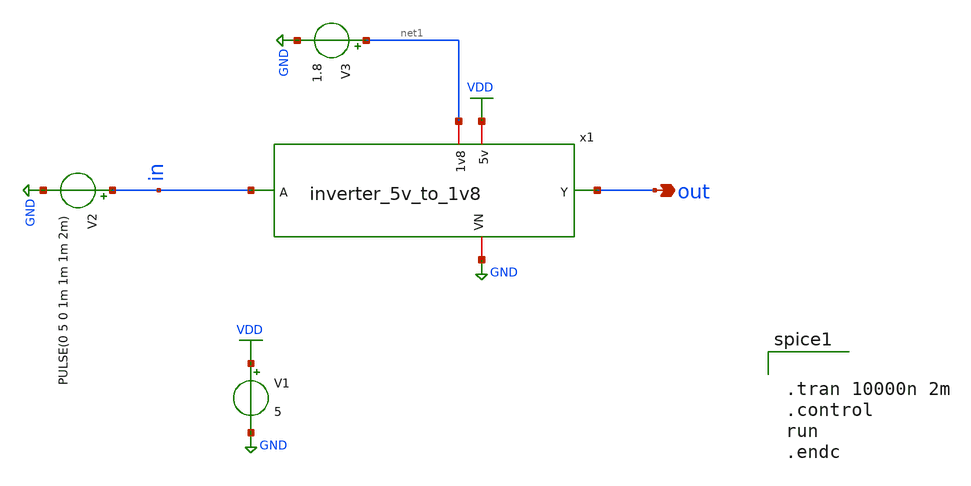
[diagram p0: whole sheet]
** sch_path: ADC/16bit_C2C/MagicAndSpice/inverter_5v_to_1v8_TB.sch
**.subckt inverter_5v_to_1v8_TB out
*.opin out
V1 VDD GND 5
V2 in GND PULSE(0 5 0 1m 1m 1m 2m)
x1 net1 VDD out in GND inverter_5v_to_1v8
V3 net1 GND 1.8
**** begin user architecture code
 .lib $::SKYWATER_MODELS/sky130.lib.spice tt


.tran 10000n 2m
.control
run
.endc

**** end user architecture code
**.ends

* expanding   symbol:  /home/ee431/workspace/6SAR_CDAC/inverter_5v_to_1v8.sym # of pins=5
** sym_path: ADC/16bit_C2C/MagicAndSpice/inverter_5v_to_1v8.sym
** sch_path: ADC/16bit_C2C/MagicAndSpice/inverter_5v_to_1v8.sch
.subckt inverter_5v_to_1v8 1v8 5v Y A VN
*.ipin A
*.opin Y
*.iopin 1v8
*.iopin VN
*.iopin 5v
XM6 Y A VN VN sky130_fd_pr__nfet_g5v0d10v5 L=0.5 W=10 nf=1 ad='int((nf+1)/2) * W/nf * 0.29' as='int((nf+2)/2) * W/nf * 0.29'
+ pd='2*int((nf+1)/2) * (W/nf + 0.29)' ps='2*int((nf+2)/2) * (W/nf + 0.29)' nrd='0.29 / W' nrs='0.29 / W'
+ sa=0 sb=0 sd=0 mult=1 m=1
XM11 Y A 1v8 5v sky130_fd_pr__pfet_g5v0d10v5 L=0.5 W=10 nf=1 ad='int((nf+1)/2) * W/nf * 0.29' as='int((nf+2)/2) * W/nf * 0.29'
+ pd='2*int((nf+1)/2) * (W/nf + 0.29)' ps='2*int((nf+2)/2) * (W/nf + 0.29)' nrd='0.29 / W' nrs='0.29 / W'
+ sa=0 sb=0 sd=0 mult=1 m=1
.ends

.GLOBAL GND
.GLOBAL VDD
.end
